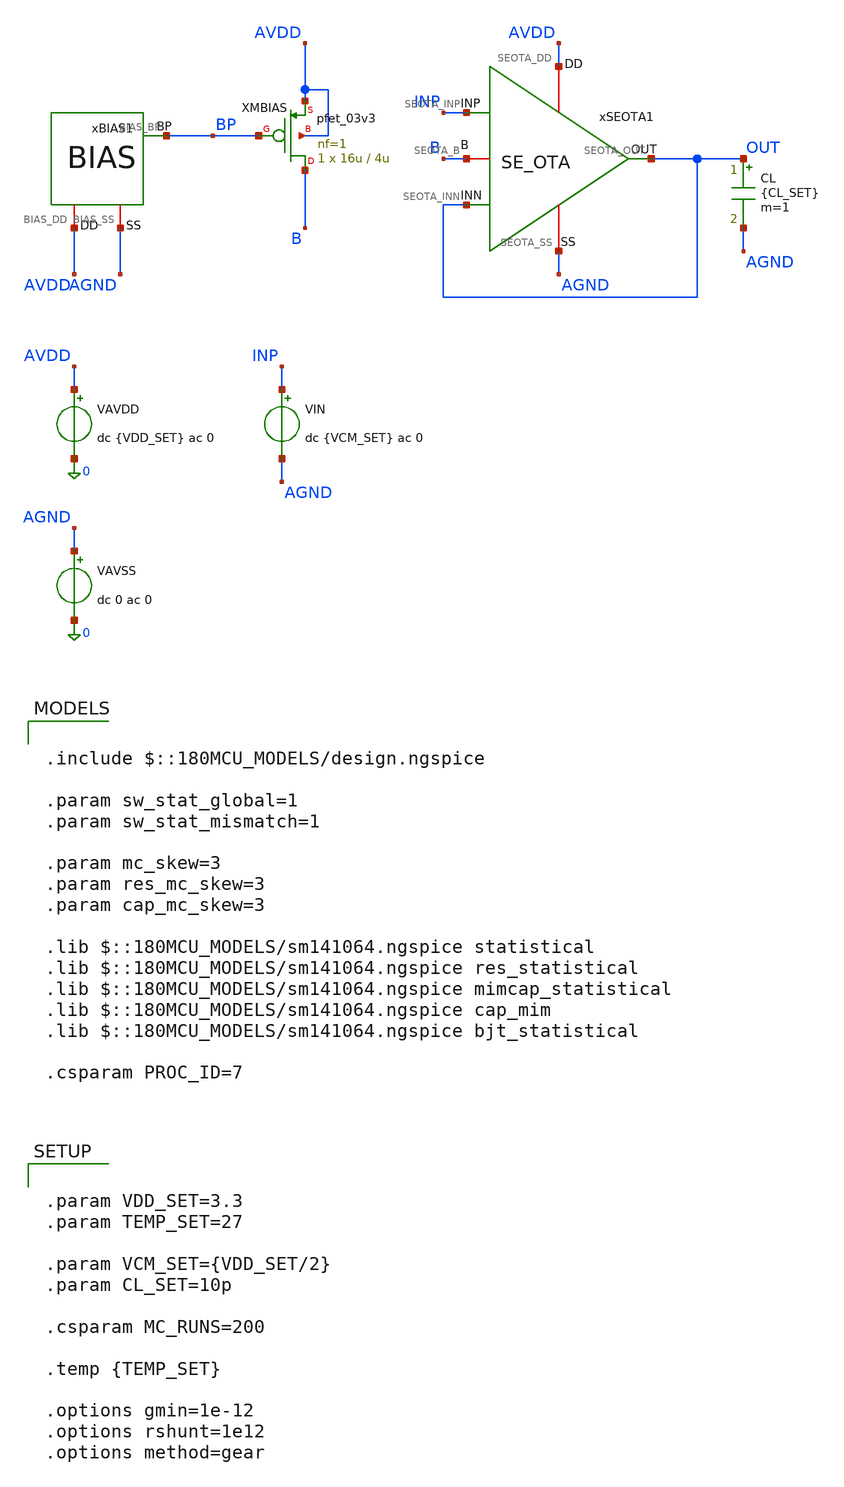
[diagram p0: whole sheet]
** sch_path: Design_Files/IC Design/Testbench/ANALOG_BLOCKS/SE_OTA/Close_Loop/SE_OTA_TB_CL_FULL.sch
**.subckt SE_OTA_TB_CL_FULL
CL OUT AGND {CL_SET} m=1
xSEOTA1 AVDD AGND INP OUT OUT B SE_OTA
VAVDD AVDD 0 dc {VDD_SET} ac 0
.save i(vavdd)
VIN INP AGND dc {VCM_SET} ac 0
VAVSS AGND 0 dc 0 ac 0
xBIAS1 AVDD AGND BP BIAS
XMBIAS B BP AVDD AVDD pfet_03v3 L=4u W=16u nf=1 ad='int((nf+1)/2) * W/nf * 0.18u' as='int((nf+2)/2) * W/nf * 0.18u'
+ pd='2*int((nf+1)/2) * (W/nf + 0.18u)' ps='2*int((nf+2)/2) * (W/nf + 0.18u)' nrd='0.18u / W' nrs='0.18u / W'
+ sa=0 sb=0 sd=0 m=1
**** begin user architecture code

.include $::180MCU_MODELS/design.ngspice

.param sw_stat_global=1
.param sw_stat_mismatch=1

.param mc_skew=3
.param res_mc_skew=3
.param cap_mc_skew=3

.lib $::180MCU_MODELS/sm141064.ngspice statistical
.lib $::180MCU_MODELS/sm141064.ngspice res_statistical
.lib $::180MCU_MODELS/sm141064.ngspice mimcap_statistical
.lib $::180MCU_MODELS/sm141064.ngspice cap_mim
.lib $::180MCU_MODELS/sm141064.ngspice bjt_statistical

.csparam PROC_ID=7




.control

destroy all

set noaskquit
set wr_singlescale
unset wr_vecnames

option klu
option numdgt=15
option method=gear
option maxord=2
option plotwinsize=0


if $&PROC_ID = 5
set proc=MM
else
if $&PROC_ID = 6
set proc=GL
else
set proc=FULL
end
end


shell mkdir -p /foss/designs/ECG_Acquisition_IC/Measurement_Results/IC_Simulation/ANALOG_BLOCKS/SE_OTA/{$proc}.Result_txt

shell rm -f /foss/designs/ECG_Acquisition_IC/Measurement_Results/IC_Simulation/ANALOG_BLOCKS/SE_OTA/{$proc}.Result_txt/{$proc}.cl_mc_summary.txt
shell rm -f /foss/designs/ECG_Acquisition_IC/Measurement_Results/IC_Simulation/ANALOG_BLOCKS/SE_OTA/{$proc}.Result_txt/{$proc}.cl_mc_debug_op.txt


echo run vos_V vout_V out_error_V cl_gain_10 b_V ibias_A idd_A power_W > /foss/designs/ECG_Acquisition_IC/Measurement_Results/IC_Simulation/ANALOG_BLOCKS/SE_OTA/{$proc}.Result_txt/{$proc}.cl_mc_summary.txt

echo run vin_V vout_V vos_V net1_V net2_V net3_V net4_V b_V ibias_A idd_A power_W > /foss/designs/ECG_Acquisition_IC/Measurement_Results/IC_Simulation/ANALOG_BLOCKS/SE_OTA/{$proc}.Result_txt/{$proc}.cl_mc_debug_op.txt


let run=1
let mc_runs=$&MC_RUNS


dowhile run <= mc_runs


set runnum=$&run

setseed $runnum
mc_source

option klu
option numdgt=15
option method=gear
option maxord=2
option plotwinsize=0

save all
save @m.xmbias.m0[id]


* OP

op

let vin_op=v(INP)-v(AGND)
let vout_op=v(OUT)-v(AGND)

let vos=vin_op-vout_op
let out_error=vout_op-vin_op

let b_op=v(B)-v(AGND)

let net1_op=v(xseota1.net1)-v(AGND)
let net2_op=v(xseota1.net2)-v(AGND)
let net3_op=v(xseota1.net3)-v(AGND)
let net4_op=v(xseota1.net4)-v(AGND)

let ibias=abs(@m.xmbias.m0[id])
let idd_total=abs(vavdd#branch)
let power_total=(v(AVDD)-v(AGND))*idd_total


set vin_val=$&vin_op
set vout_val=$&vout_op

set vos_val=$&vos
set out_error_val=$&out_error

set b_val=$&b_op

set net1_val=$&net1_op
set net2_val=$&net2_op
set net3_val=$&net3_op
set net4_val=$&net4_op

set ibias_val=$&ibias
set idd_val=$&idd_total
set power_val=$&power_total


echo $runnum $vin_val $vout_val $vos_val $net1_val $net2_val $net3_val $net4_val $b_val $ibias_val $idd_val
+ $power_val >> /foss/designs/ECG_Acquisition_IC/Measurement_Results/IC_Simulation/ANALOG_BLOCKS/SE_OTA/{$proc}.Result_txt/{$proc}.cl_mc_debug_op.txt


destroy all


* CLOSED-LOOP AC

alter @VIN[ACMAG]=1
alter @VIN[ACPHASE]=0

ac dec 100 0.1 10Meg

let vin_ac=v(INP)-v(AGND)
let vout_ac=v(OUT)-v(AGND)

let cl_tf=vout_ac/vin_ac
let cl_gain=mag(cl_tf)

meas ac cl_gain_10 find cl_gain at=10

set cl_gain_val=$&cl_gain_10


* SUMMARY

echo $runnum $vos_val $vout_val $out_error_val $cl_gain_val $b_val $ibias_val $idd_val $power_val >>
+ /foss/designs/ECG_Acquisition_IC/Measurement_Results/IC_Simulation/ANALOG_BLOCKS/SE_OTA/{$proc}.Result_txt/{$proc}.cl_mc_summary.txt


destroy all

let run=run+1


end


quit

.endc




.param VDD_SET=3.3
.param TEMP_SET=27

.param VCM_SET={VDD_SET/2}
.param CL_SET=10p

.csparam MC_RUNS=200

.temp {TEMP_SET}

.options gmin=1e-12
.options rshunt=1e12
.options method=gear


**** end user architecture code
**.ends

* expanding   symbol:  ECG_Acquisition_IC/Design_Files/IC
*+ Design/Schematic/ANALOG_BLOCKS/SE_OTA/SE_OTA.sym # of pins=6
** sym_path: Design_Files/IC Design/Schematic/SE_OTA/SE_OTA.sym
** sch_path: Design_Files/IC Design/Schematic/SE_OTA/SE_OTA.sch
.subckt SE_OTA SEOTA_DD SEOTA_SS SEOTA_INP SEOTA_INN SEOTA_OUT SEOTA_B
*.iopin SEOTA_DD
*.iopin SEOTA_SS
*.ipin SEOTA_INP
*.ipin SEOTA_INN
*.opin SEOTA_OUT
*.iopin SEOTA_B
XM3 net4 net4 SEOTA_DD SEOTA_DD pfet_03v3 L=4u W=1u nf=1 ad='int((nf+1)/2) * W/nf * 0.18u' as='int((nf+2)/2) * W/nf * 0.18u'
+ pd='2*int((nf+1)/2) * (W/nf + 0.18u)' ps='2*int((nf+2)/2) * (W/nf + 0.18u)' nrd='0.18u / W' nrs='0.18u / W'
+ sa=0 sb=0 sd=0 m=60
XM7 SEOTA_OUT SEOTA_B SEOTA_SS SEOTA_SS nfet_03v3 L=0.5u W=1u nf=1 ad='int((nf+1)/2) * W/nf * 0.18u'
+ as='int((nf+2)/2) * W/nf * 0.18u' pd='2*int((nf+1)/2) * (W/nf + 0.18u)' ps='2*int((nf+2)/2) * (W/nf + 0.18u)'
+ nrd='0.18u / W' nrs='0.18u / W' sa=0 sb=0 sd=0 m=100
Rz net1 net2 3.8k m=1
XM5 net3 SEOTA_B SEOTA_SS SEOTA_SS nfet_03v3 L=2u W=1u nf=1 ad='int((nf+1)/2) * W/nf * 0.18u' as='int((nf+2)/2) * W/nf * 0.18u'
+ pd='2*int((nf+1)/2) * (W/nf + 0.18u)' ps='2*int((nf+2)/2) * (W/nf + 0.18u)' nrd='0.18u / W' nrs='0.18u / W'
+ sa=0 sb=0 sd=0 m=10
XM6 SEOTA_OUT net1 SEOTA_DD SEOTA_DD pfet_03v3 L=0.5u W=1u nf=1 ad='int((nf+1)/2) * W/nf * 0.18u' as='int((nf+2)/2) * W/nf * 0.18u'
+ pd='2*int((nf+1)/2) * (W/nf + 0.18u)' ps='2*int((nf+2)/2) * (W/nf + 0.18u)' nrd='0.18u / W' nrs='0.18u / W'
+ sa=0 sb=0 sd=0 m=400
XM8 SEOTA_B SEOTA_B SEOTA_SS SEOTA_SS nfet_03v3 L=2u W=1u nf=1 ad='int((nf+1)/2) * W/nf * 0.18u' as='int((nf+2)/2) * W/nf * 0.18u'
+ pd='2*int((nf+1)/2) * (W/nf + 0.18u)' ps='2*int((nf+2)/2) * (W/nf + 0.18u)' nrd='0.18u / W' nrs='0.18u / W'
+ sa=0 sb=0 sd=0 m=20
Cc net2 SEOTA_OUT 2p m=1
XM4 net1 net4 SEOTA_DD SEOTA_DD pfet_03v3 L=4u W=1u nf=1 ad='int((nf+1)/2) * W/nf * 0.18u' as='int((nf+2)/2) * W/nf * 0.18u'
+ pd='2*int((nf+1)/2) * (W/nf + 0.18u)' ps='2*int((nf+2)/2) * (W/nf + 0.18u)' nrd='0.18u / W' nrs='0.18u / W'
+ sa=0 sb=0 sd=0 m=60
XM1 net4 SEOTA_INN net3 SEOTA_SS nfet_03v3 L=4u W=1u nf=1 ad='int((nf+1)/2) * W/nf * 0.18u' as='int((nf+2)/2) * W/nf * 0.18u'
+ pd='2*int((nf+1)/2) * (W/nf + 0.18u)' ps='2*int((nf+2)/2) * (W/nf + 0.18u)' nrd='0.18u / W' nrs='0.18u / W'
+ sa=0 sb=0 sd=0 m=400
XM2 net1 SEOTA_INP net3 SEOTA_SS nfet_03v3 L=4u W=1u nf=1 ad='int((nf+1)/2) * W/nf * 0.18u' as='int((nf+2)/2) * W/nf * 0.18u'
+ pd='2*int((nf+1)/2) * (W/nf + 0.18u)' ps='2*int((nf+2)/2) * (W/nf + 0.18u)' nrd='0.18u / W' nrs='0.18u / W'
+ sa=0 sb=0 sd=0 m=400
.ends


* expanding   symbol:  ECG_Acquisition_IC/Design_Files/IC Design/Schematic/AFE_BLOCKS/BIAS/BIAS.sym
*+ # of pins=3
** sym_path: Design_Files/IC Design/Schematic/AFE_BLOCKS/BIAS/BIAS.sym
** sch_path: Design_Files/IC Design/Schematic/AFE_BLOCKS/BIAS/BIAS.sch
.subckt BIAS BIAS_DD BIAS_SS BIAS_BP
*.iopin BIAS_DD
*.iopin BIAS_SS
*.opin BIAS_BP
XMN2 BIAS_BP net2 net1 BIAS_SS nfet_03v3 L=4u W=16u nf=1 ad='int((nf+1)/2) * W/nf * 0.18u' as='int((nf+2)/2) * W/nf * 0.18u'
+ pd='2*int((nf+1)/2) * (W/nf + 0.18u)' ps='2*int((nf+2)/2) * (W/nf + 0.18u)' nrd='0.18u / W' nrs='0.18u / W'
+ sa=0 sb=0 sd=0 m=1
XMP2 BIAS_BP BIAS_BP BIAS_DD BIAS_DD pfet_03v3 L=4u W=16u nf=1 ad='int((nf+1)/2) * W/nf * 0.18u' as='int((nf+2)/2) * W/nf * 0.18u'
+ pd='2*int((nf+1)/2) * (W/nf + 0.18u)' ps='2*int((nf+2)/2) * (W/nf + 0.18u)' nrd='0.18u / W' nrs='0.18u / W'
+ sa=0 sb=0 sd=0 m=1
XMN1 net2 net2 net3 BIAS_SS nfet_03v3 L=4u W=24u nf=1 ad='int((nf+1)/2) * W/nf * 0.18u' as='int((nf+2)/2) * W/nf * 0.18u'
+ pd='2*int((nf+1)/2) * (W/nf + 0.18u)' ps='2*int((nf+2)/2) * (W/nf + 0.18u)' nrd='0.18u / W' nrs='0.18u / W'
+ sa=0 sb=0 sd=0 m=1
XMP1 net2 BIAS_BP BIAS_DD BIAS_DD pfet_03v3 L=4u W=16u nf=1 ad='int((nf+1)/2) * W/nf * 0.18u' as='int((nf+2)/2) * W/nf * 0.18u'
+ pd='2*int((nf+1)/2) * (W/nf + 0.18u)' ps='2*int((nf+2)/2) * (W/nf + 0.18u)' nrd='0.18u / W' nrs='0.18u / W'
+ sa=0 sb=0 sd=0 m=1
XMST BIAS_BP BIAS_BP net2 BIAS_SS nfet_03v3 L=10u W=0.5u nf=1 ad='int((nf+1)/2) * W/nf * 0.18u' as='int((nf+2)/2) * W/nf * 0.18u'
+ pd='2*int((nf+1)/2) * (W/nf + 0.18u)' ps='2*int((nf+2)/2) * (W/nf + 0.18u)' nrd='0.18u / W' nrs='0.18u / W'
+ sa=0 sb=0 sd=0 m=1
XQ1 BIAS_SS BIAS_SS net3 pnp_05p00x00p42 m=1 par=1
XQ2 BIAS_SS BIAS_SS net4 pnp_05p00x00p42 m=30 par=30
XRS net4 net1 BIAS_SS nwell r_width=3e-6 r_length=1.522e-6 m=1
.ends

.end
